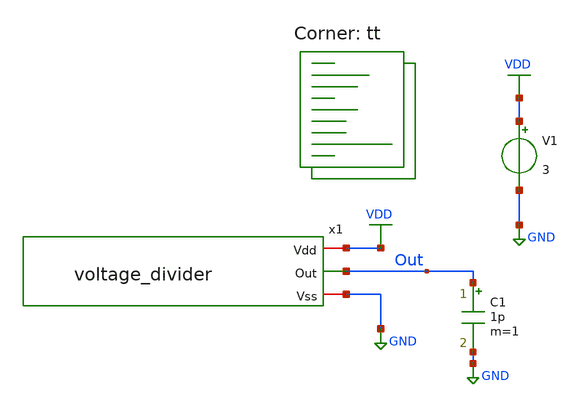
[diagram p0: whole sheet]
** sch_path: voltage_divider_back/xschem/voltage_divider_tb.sch
**.subckt voltage_divider_tb
x1 VDD Out GND voltage_divider
C1 Out GND 1p m=1
V1 VDD GND 3
**** begin user architecture code

** opencircuitdesign pdks install
.lib $::SKYWATER_MODELS/sky130.lib.spice tt


.lib $::SKYWATER_MODELS/sky130.lib.spice tt



.control
tran 1n 80u
plot VDD Out
save all
.endc



**** end user architecture code
**.ends

* expanding   symbol:  voltage_divider.sym # of pins=3
** sym_path: xschem/voltage_divider.sym
** sch_path: xschem/voltage_divider.sch
.subckt voltage_divider Vdd Out Vss
*.opin Out
*.iopin Vdd
*.iopin Vss
XR1 Out Vdd sky130_fd_pr__res_generic_po W=.33 L=10 m=1
XR2 Vss Out sky130_fd_pr__res_generic_po W=.33 L=10 m=1
.ends

.GLOBAL VDD
.GLOBAL GND
.end
